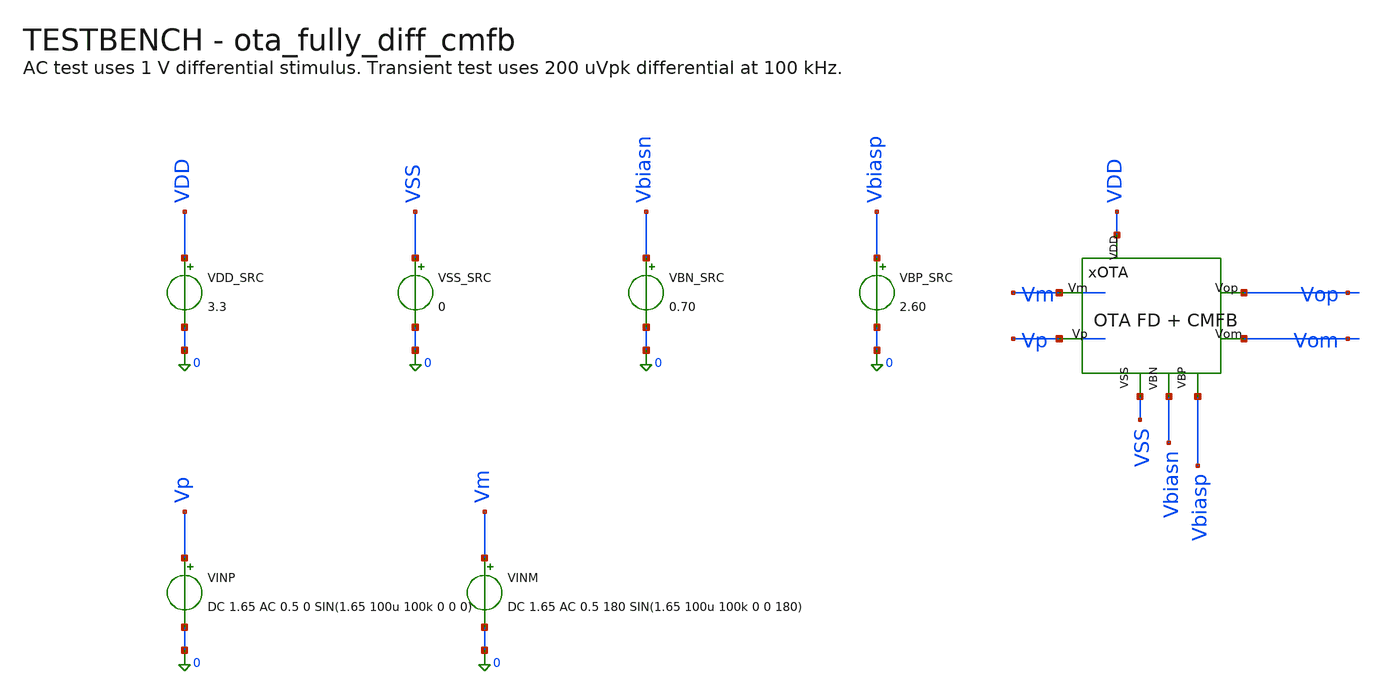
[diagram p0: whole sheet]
** sch_path: src/schematics/TEMPORARY/ota_fully_diff_cmfb_tb.sch
**.subckt ota_fully_diff_cmfb_tb
VDD_SRC VDD 0 3.3
.save i(vdd_src)
VSS_SRC VSS 0 0
.save i(vss_src)
VBN_SRC Vbiasn 0 0.70
.save i(vbn_src)
VBP_SRC Vbiasp 0 2.60
.save i(vbp_src)
VINP Vp 0 DC 1.65 AC 0.5 0 SIN(1.65 100u 100k 0 0 0)
VINM Vm 0 DC 1.65 AC 0.5 180 SIN(1.65 100u 100k 0 0 180)
xOTA Vm Vp Vop Vom VDD VSS Vbiasn Vbiasp ota_fully_diff_cmfb
**** begin user architecture code


.lib /foss/pdks/gf180mcuD/libs.tech/ngspice/sm141064.ngspice typical
.inc /foss/pdks/gf180mcuD/libs.tech/ngspice/design.ngspice

CLP Vop VSS 0.5p
CLM Vom VSS 0.5p
RLP Vop VSS 100Meg
RLM Vom VSS 100Meg

.control
set color0=white
set color1=black
save all
op
print v(Vp) v(Vm) v(Vop) v(Vom)

ac dec 100 10 1G
let vid_ac = v(Vp)-v(Vm)
let vod_ac = v(Vop)-v(Vom)
let av_diff_db = db(vod_ac/vid_ac)
let av_cm_db = db((v(Vop)+v(Vom))/2)
plot av_diff_db av_cm_db

tran 2n 50u
let vid = v(Vp)-v(Vm)
let vod = v(Vop)-v(Vom)
let vocm = (v(Vop)+v(Vom))/2
meas tran vocm_avg AVG vocm from=10u to=50u
meas tran vocm_min MIN vocm from=10u to=50u
meas tran vocm_max MAX vocm from=10u to=50u
meas tran vod_pp PP vod from=10u to=50u
plot vid vod
plot v(Vop) v(Vom)
plot vocm
write ota_fully_diff_cmfb_tb.raw v(Vp) v(Vm) v(Vop) v(Vom)
.endc
.end


**** end user architecture code
**.ends

* expanding   symbol:
*+  /foss/designs/low-power-12b-first-order-delta-sigma-adc/src/schematics/TEMPORARY/ota_fully_diff_cmfb.sym # of pins=8
** sym_path: src/schematics/TEMPORARY/ota_fully_diff_cmfb.sym
** sch_path: src/schematics/TEMPORARY/ota_fully_diff_cmfb.sch
.subckt ota_fully_diff_cmfb Vm Vp Vop Vom VDD VSS Vbiasn Vbiasp
*.ipin Vp
*.ipin Vm
*.opin Vop
*.opin Vom
*.ipin VDD
*.ipin VSS
*.ipin Vbiasn
*.ipin Vbiasp
XM1P net6 net7 net8 VDD pfet_03v3 L=1u W=24u nf=2 ad='int((nf+1)/2) * W/nf * 0.18u' as='int((nf+2)/2) * W/nf * 0.18u'
+ pd='2*int((nf+1)/2) * (W/nf + 0.18u)' ps='2*int((nf+2)/2) * (W/nf + 0.18u)' nrd='0.18u / W' nrs='0.18u / W'
+ sa=0 sb=0 sd=0 m=1
XM2P net9 net10 net11 VDD pfet_03v3 L=1u W=24u nf=2 ad='int((nf+1)/2) * W/nf * 0.18u' as='int((nf+2)/2) * W/nf * 0.18u'
+ pd='2*int((nf+1)/2) * (W/nf + 0.18u)' ps='2*int((nf+2)/2) * (W/nf + 0.18u)' nrd='0.18u / W' nrs='0.18u / W'
+ sa=0 sb=0 sd=0 m=1
XM1N net12 net13 net14 VSS nfet_03v3 L=0.6u W=24u nf=2 ad='int((nf+1)/2) * W/nf * 0.18u' as='int((nf+2)/2) * W/nf * 0.18u'
+ pd='2*int((nf+1)/2) * (W/nf + 0.18u)' ps='2*int((nf+2)/2) * (W/nf + 0.18u)' nrd='0.18u / W' nrs='0.18u / W'
+ sa=0 sb=0 sd=0 m=1
XM2N net15 net16 net17 VSS nfet_03v3 L=0.6u W=24u nf=2 ad='int((nf+1)/2) * W/nf * 0.18u' as='int((nf+2)/2) * W/nf * 0.18u'
+ pd='2*int((nf+1)/2) * (W/nf + 0.18u)' ps='2*int((nf+2)/2) * (W/nf + 0.18u)' nrd='0.18u / W' nrs='0.18u / W'
+ sa=0 sb=0 sd=0 m=1
XMTAIL1 net18 net19 net20 VSS nfet_03v3 L=1u W=20u nf=2 ad='int((nf+1)/2) * W/nf * 0.18u' as='int((nf+2)/2) * W/nf * 0.18u'
+ pd='2*int((nf+1)/2) * (W/nf + 0.18u)' ps='2*int((nf+2)/2) * (W/nf + 0.18u)' nrd='0.18u / W' nrs='0.18u / W'
+ sa=0 sb=0 sd=0 m=1
XM3P net21 net22 net23 VDD pfet_03v3 L=1u W=48u nf=4 ad='int((nf+1)/2) * W/nf * 0.18u' as='int((nf+2)/2) * W/nf * 0.18u'
+ pd='2*int((nf+1)/2) * (W/nf + 0.18u)' ps='2*int((nf+2)/2) * (W/nf + 0.18u)' nrd='0.18u / W' nrs='0.18u / W'
+ sa=0 sb=0 sd=0 m=1
XM4P net24 net25 net26 VDD pfet_03v3 L=1u W=48u nf=4 ad='int((nf+1)/2) * W/nf * 0.18u' as='int((nf+2)/2) * W/nf * 0.18u'
+ pd='2*int((nf+1)/2) * (W/nf + 0.18u)' ps='2*int((nf+2)/2) * (W/nf + 0.18u)' nrd='0.18u / W' nrs='0.18u / W'
+ sa=0 sb=0 sd=0 m=1
XM3N net27 net28 net29 VSS nfet_03v3 L=0.6u W=36u nf=3 ad='int((nf+1)/2) * W/nf * 0.18u' as='int((nf+2)/2) * W/nf * 0.18u'
+ pd='2*int((nf+1)/2) * (W/nf + 0.18u)' ps='2*int((nf+2)/2) * (W/nf + 0.18u)' nrd='0.18u / W' nrs='0.18u / W'
+ sa=0 sb=0 sd=0 m=1
XM4N net30 net31 net32 VSS nfet_03v3 L=0.6u W=36u nf=3 ad='int((nf+1)/2) * W/nf * 0.18u' as='int((nf+2)/2) * W/nf * 0.18u'
+ pd='2*int((nf+1)/2) * (W/nf + 0.18u)' ps='2*int((nf+2)/2) * (W/nf + 0.18u)' nrd='0.18u / W' nrs='0.18u / W'
+ sa=0 sb=0 sd=0 m=1
XMTAIL2 net33 net34 net35 VSS nfet_03v3 L=1u W=24u nf=2 ad='int((nf+1)/2) * W/nf * 0.18u' as='int((nf+2)/2) * W/nf * 0.18u'
+ pd='2*int((nf+1)/2) * (W/nf + 0.18u)' ps='2*int((nf+2)/2) * (W/nf + 0.18u)' nrd='0.18u / W' nrs='0.18u / W'
+ sa=0 sb=0 sd=0 m=1
RZP net4 N1 1k m=1
CCP Vop net4 350f m=1
RZM net5 N2 1k m=1
CCM Vom net5 350f m=1
RSENP VCM_SENSE Vop 500k m=1
RSENM VCM_SENSE Vom 500k m=1
XMCM1P net36 net37 net38 VDD pfet_03v3 L=1u W=8u nf=1 ad='int((nf+1)/2) * W/nf * 0.18u' as='int((nf+2)/2) * W/nf * 0.18u'
+ pd='2*int((nf+1)/2) * (W/nf + 0.18u)' ps='2*int((nf+2)/2) * (W/nf + 0.18u)' nrd='0.18u / W' nrs='0.18u / W'
+ sa=0 sb=0 sd=0 m=1
XMCM2P net39 net40 net41 VDD pfet_03v3 L=1u W=8u nf=1 ad='int((nf+1)/2) * W/nf * 0.18u' as='int((nf+2)/2) * W/nf * 0.18u'
+ pd='2*int((nf+1)/2) * (W/nf + 0.18u)' ps='2*int((nf+2)/2) * (W/nf + 0.18u)' nrd='0.18u / W' nrs='0.18u / W'
+ sa=0 sb=0 sd=0 m=1
XMCM1N net42 net43 net44 VSS nfet_03v3 L=1u W=6u nf=1 ad='int((nf+1)/2) * W/nf * 0.18u' as='int((nf+2)/2) * W/nf * 0.18u'
+ pd='2*int((nf+1)/2) * (W/nf + 0.18u)' ps='2*int((nf+2)/2) * (W/nf + 0.18u)' nrd='0.18u / W' nrs='0.18u / W'
+ sa=0 sb=0 sd=0 m=1
XMCM2N net45 net46 net47 VSS nfet_03v3 L=1u W=6u nf=1 ad='int((nf+1)/2) * W/nf * 0.18u' as='int((nf+2)/2) * W/nf * 0.18u'
+ pd='2*int((nf+1)/2) * (W/nf + 0.18u)' ps='2*int((nf+2)/2) * (W/nf + 0.18u)' nrd='0.18u / W' nrs='0.18u / W'
+ sa=0 sb=0 sd=0 m=1
XMTAILCM net48 net49 net50 VSS nfet_03v3 L=1u W=5u nf=1 ad='int((nf+1)/2) * W/nf * 0.18u' as='int((nf+2)/2) * W/nf * 0.18u'
+ pd='2*int((nf+1)/2) * (W/nf + 0.18u)' ps='2*int((nf+2)/2) * (W/nf + 0.18u)' nrd='0.18u / W' nrs='0.18u / W'
+ sa=0 sb=0 sd=0 m=1
RREFH VDD VCM_INT 200k m=1
RREFL VCM_INT VSS 200k m=1
CREF VCM_INT VSS 2p m=1
CCMFB VCM_CTRL VSS 1p m=1
RSTART VCM_CTRL Vbiasp 50Meg m=1
.ends

.end
